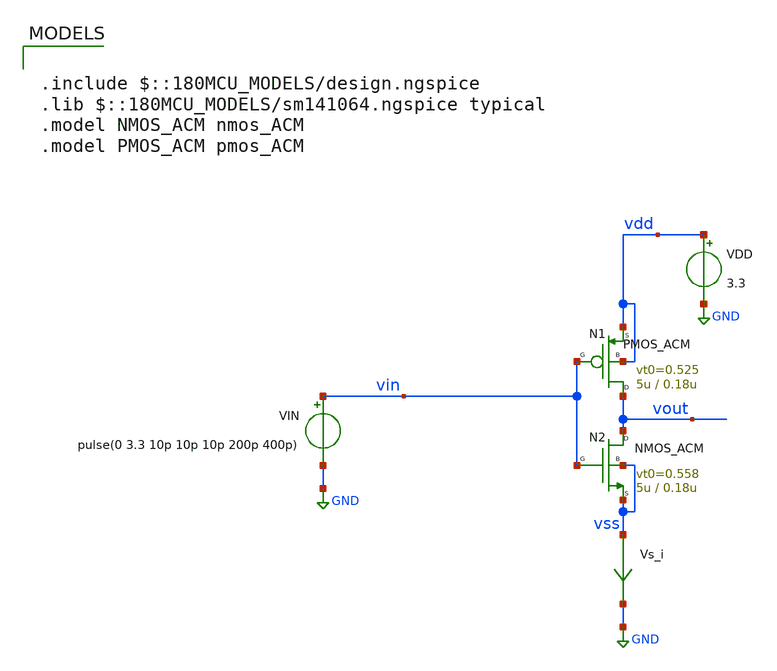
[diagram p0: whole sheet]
** sch_path: Examples/GF180MCU/xschem/TB_inv_acm.sch
**.subckt TB_inv_acm
N2 vout vin vss vss NMOS_ACM w=5u l=0.18u n=1.37 is=5.52u vt0=0.558 sigma=27m zeta=56m
VIN vin GND pulse(0 3.3 10p 10p 10p 200p 400p)
VDD vdd GND 3.3
N1 vout vin vdd vdd PMOS_ACM w=5u l=0.18u n=1.40 is=1.82u vt0=0.525 sigma=24m zeta=35m
Vs_i vss GND 0
.save i(vs_i)
**** begin user architecture code

.include $::180MCU_MODELS/design.ngspice
.lib $::180MCU_MODELS/sm141064.ngspice typical
.model NMOS_ACM nmos_ACM
.model PMOS_ACM pmos_ACM



.option gmin=1e-18
.control
pre_osdi /home/gmaranhao/Documents/MOSFET_model/Examples/GF180MCU/xschem/symbol/NMOS_ACM_2V0.osdi
pre_osdi /home/gmaranhao/Documents/MOSFET_model/Examples/GF180MCU/xschem/symbol/PMOS_ACM_2V0.osdi
save all

tran 1p 1n
write TB_inv_acm.raw
set appendwrite

dc VIN 0 3.3 1m
remzerovec
write TB_inv_acm.raw

.endc


**** end user architecture code
**.ends
.GLOBAL GND
.end
